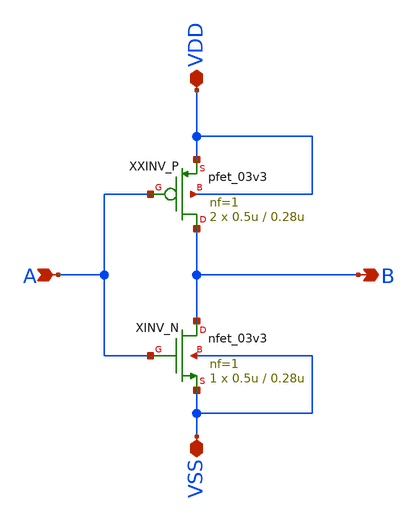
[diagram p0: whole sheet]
** sch_path: designs/sar_adc/samplehold/gate_inv_sh/xschem/gate_inv_sh.sch
**.subckt gate_inv_sh B A VDD VSS
*.opin B
*.ipin A
*.iopin VDD
*.iopin VSS
XINV_N B A VSS VSS nfet_03v3 L=0.28u W=0.5u nf=1 ad='int((nf+1)/2) * W/nf * 0.18u' as='int((nf+2)/2) * W/nf * 0.18u'
+ pd='2*int((nf+1)/2) * (W/nf + 0.18u)' ps='2*int((nf+2)/2) * (W/nf + 0.18u)' nrd='0.18u / W' nrs='0.18u / W'
+ sa=0 sb=0 sd=0 m=1
XXINV_P B A VDD VDD pfet_03v3 L=0.28u W=0.5u nf=1 ad='int((nf+1)/2) * W/nf * 0.18u' as='int((nf+2)/2) * W/nf * 0.18u'
+ pd='2*int((nf+1)/2) * (W/nf + 0.18u)' ps='2*int((nf+2)/2) * (W/nf + 0.18u)' nrd='0.18u / W' nrs='0.18u / W'
+ sa=0 sb=0 sd=0 m=2
**.ends
.end
